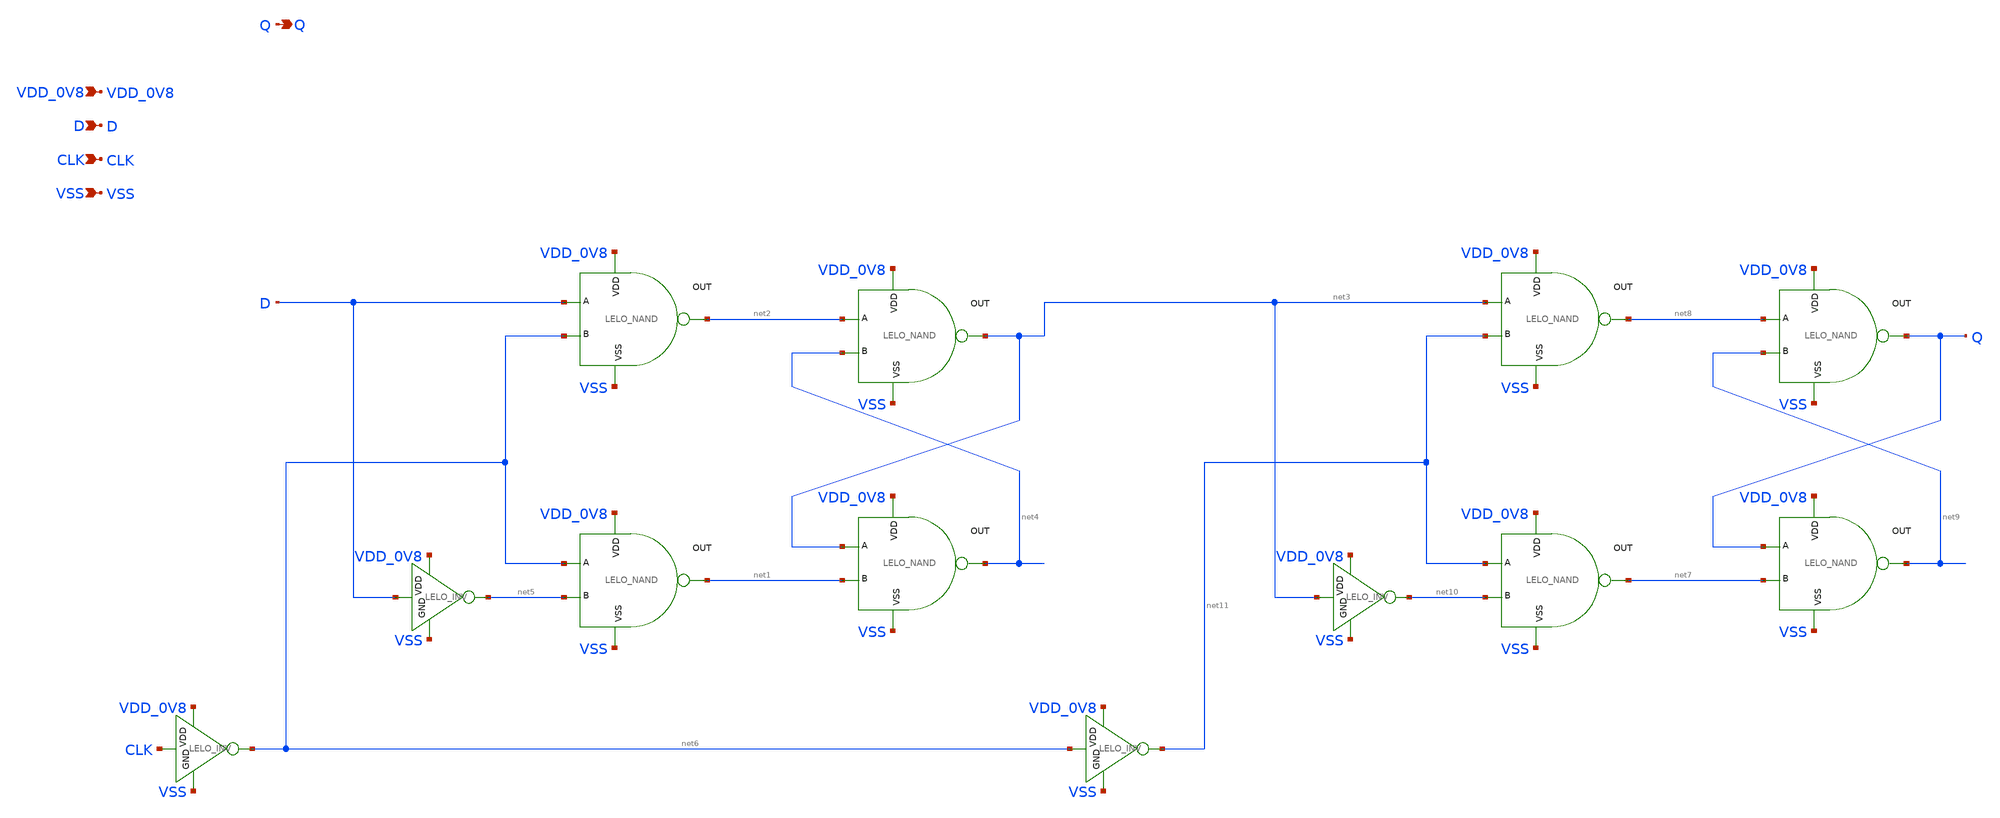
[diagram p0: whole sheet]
** sch_path: design/LELO_SVOD_SKY130A/LELO_DFF.sch
**.subckt LELO_DFF VDD_0V8 VSS CLK D Q
*.ipin VDD_0V8
*.ipin VSS
*.ipin CLK
*.ipin D
*.opin Q
x1 VDD_0V8 net2 D net6 VSS LELO_NAND
x2 VDD_0V8 net1 net6 net5 VSS LELO_NAND
x3 VDD_0V8 net4 net3 net1 VSS LELO_NAND
x4 VDD_0V8 net3 net2 net4 VSS LELO_NAND
x9 VDD_0V8 D net5 VSS LELO_INV
x11 VDD_0V8 CLK net6 VSS LELO_INV
x5 VDD_0V8 net8 net3 net11 VSS LELO_NAND
x6 VDD_0V8 net7 net11 net10 VSS LELO_NAND
x7 VDD_0V8 net9 Q net7 VSS LELO_NAND
x8 VDD_0V8 Q net8 net9 VSS LELO_NAND
x10 VDD_0V8 net3 net10 VSS LELO_INV
x12 VDD_0V8 net6 net11 VSS LELO_INV
**.ends

* expanding   symbol:  LELO_SVOD_SKY130A/LELO_NAND.sym # of pins=5
** sym_path: design/LELO_SVOD_SKY130A/LELO_NAND.sym
** sch_path: design/LELO_SVOD_SKY130A/LELO_NAND.sch
.subckt LELO_NAND VDD OUT A B VSS
*.ipin VDD
*.ipin VSS
*.opin OUT
*.ipin A
*.ipin B
XM1 net1 A VSS VSS sky130_fd_pr__nfet_01v8_lvt L=0.15 W=1 nf=1 ad='int((1 + 1)/2) * 1 / 1 * 0.29' as='int((1 + 2)/2) * 1 / 1 * 0.29'
+ pd='2*int((1 + 1)/2) * (1 / 1 + 0.29)' ps='2*int((1 + 2)/2) * (1 / 1 + 0.29)' nrd='0.29 / 1 ' nrs='0.29 / 1 '
+ sa=0 sb=0 sd=0 mult=1 m=1
XM2 OUT B net1 net1 sky130_fd_pr__nfet_01v8_lvt L=0.15 W=1 nf=1 ad='int((1 + 1)/2) * 1 / 1 * 0.29' as='int((1 + 2)/2) * 1 / 1 * 0.29'
+ pd='2*int((1 + 1)/2) * (1 / 1 + 0.29)' ps='2*int((1 + 2)/2) * (1 / 1 + 0.29)' nrd='0.29 / 1 ' nrs='0.29 / 1 '
+ sa=0 sb=0 sd=0 mult=1 m=1
XM3 OUT A VDD VDD sky130_fd_pr__pfet_01v8_lvt L=0.35 W=2 nf=1 ad='int((1 + 1)/2) * 2 / 1 * 0.29' as='int((1 + 2)/2) * 2 / 1 * 0.29'
+ pd='2*int((1 + 1)/2) * (2 / 1 + 0.29)' ps='2*int((1 + 2)/2) * (2 / 1 + 0.29)' nrd='0.29 / 2 ' nrs='0.29 / 2 '
+ sa=0 sb=0 sd=0 mult=1 m=1
XM4 OUT B VDD VDD sky130_fd_pr__pfet_01v8_lvt L=0.35 W=2 nf=1 ad='int((1 + 1)/2) * 2 / 1 * 0.29' as='int((1 + 2)/2) * 2 / 1 * 0.29'
+ pd='2*int((1 + 1)/2) * (2 / 1 + 0.29)' ps='2*int((1 + 2)/2) * (2 / 1 + 0.29)' nrd='0.29 / 2 ' nrs='0.29 / 2 '
+ sa=0 sb=0 sd=0 mult=1 m=1
.ends


* expanding   symbol:  LELO_SVOD_SKY130A/LELO_INV.sym # of pins=4
** sym_path: design/LELO_SVOD_SKY130A/LELO_INV.sym
** sch_path: design/LELO_SVOD_SKY130A/LELO_INV.sch
.subckt LELO_INV VDD VIN VOUT GND
*.ipin VIN
*.ipin VDD
*.ipin GND
*.opin VOUT
XM1 VOUT VIN GND GND sky130_fd_pr__nfet_01v8_lvt L=0.15 W=1 nf=1 ad='int((1 + 1)/2) * 1 / 1 * 0.29' as='int((1 + 2)/2) * 1 / 1 * 0.29'
+ pd='2*int((1 + 1)/2) * (1 / 1 + 0.29)' ps='2*int((1 + 2)/2) * (1 / 1 + 0.29)' nrd='0.29 / 1 ' nrs='0.29 / 1 '
+ sa=0 sb=0 sd=0 mult=1 m=1
XM2 VOUT VIN VDD VDD sky130_fd_pr__pfet_01v8_lvt L=0.35 W=1 nf=1 ad='int((1 + 1)/2) * 1 / 1 * 0.29' as='int((1 + 2)/2) * 1 / 1 * 0.29'
+ pd='2*int((1 + 1)/2) * (1 / 1 + 0.29)' ps='2*int((1 + 2)/2) * (1 / 1 + 0.29)' nrd='0.29 / 1 ' nrs='0.29 / 1 '
+ sa=0 sb=0 sd=0 mult=2 m=2
.ends

.end
